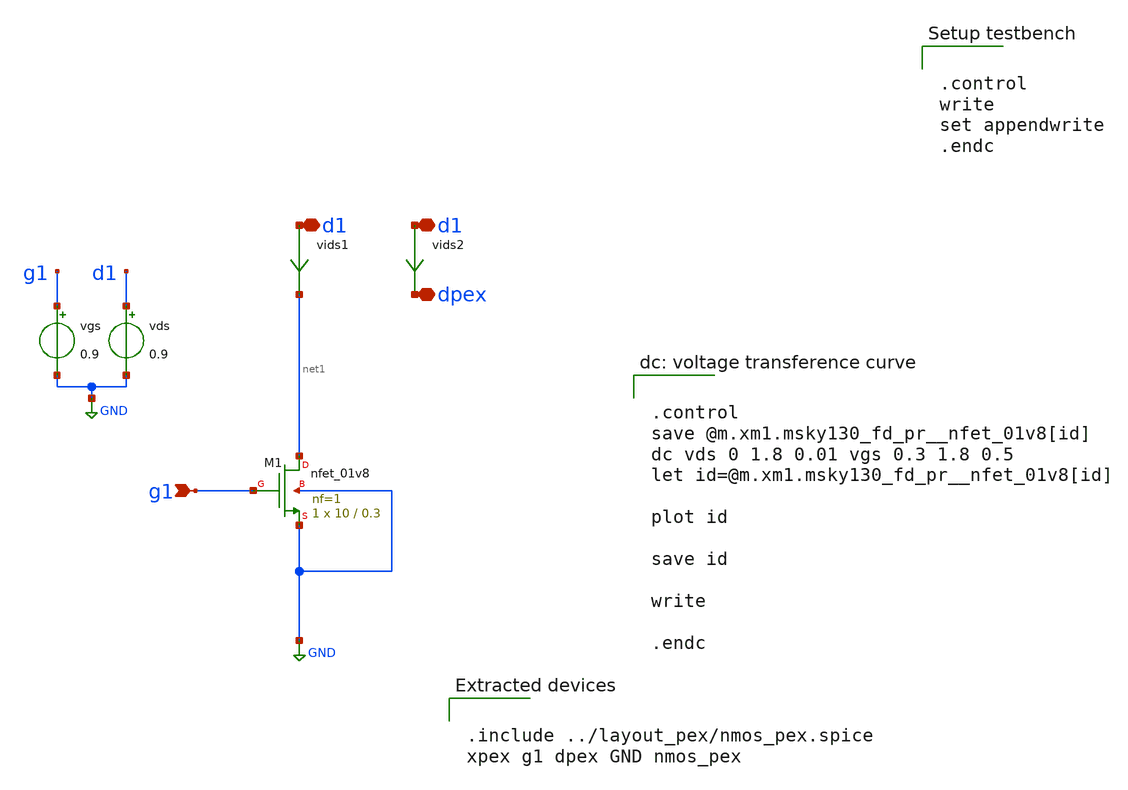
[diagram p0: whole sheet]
** sch_path: samples/digital_cosimulation/sigma_delta_counter/test/pulse_test.sch

*.lib $env(PDK_ROOT)/$env(PDK)/libs.tech/ngspice/sky130.lib.spice tt
.lib $env(PDK_ROOT)/$env(PDK)/libs.tech/ngspice/sky130.lib.spice.tt.red tt
.lib $env(PDK_ROOT)/$env(PDK)/libs.ref/sky130_fd_sc_hd/spice/sky130_fd_sc_hd.spice


.control
write
set appendwrite
.endc


**.subckt pulse_test g1 d1 d1 dpex
*.ipin g1
*.iopin d1
*.iopin d1
*.iopin dpex
XM1 net1 g1 GND GND sky130_fd_pr__nfet_01v8 L=0.3 W=10 nf=1 ad='int((nf+1)/2) * W/nf * 0.29' as='int((nf+2)/2) * W/nf * 0.29'
+ pd='2*int((nf+1)/2) * (W/nf + 0.29)' ps='2*int((nf+2)/2) * (W/nf + 0.29)' nrd='0.29 / W' nrs='0.29 / W'
+ sa=0 sb=0 sd=0 mult=1 m=1
vgs g1 GND 0.9
vds d1 GND 0.9
vids1 d1 net1 0
.save i(vids1)
vids2 d1 dpex 0
.save i(vids2)
**** begin user architecture code


.control
save @m.xm1.msky130_fd_pr__nfet_01v8[id]
dc vds 0 1.8 0.01 vgs 0.3 1.8 0.5
let id=@m.xm1.msky130_fd_pr__nfet_01v8[id]

plot id

save id

write

.endc




.include ../layout_pex/nmos_pex.spice
xpex g1 dpex GND nmos_pex


**** end user architecture code
**.ends
.GLOBAL GND
.end
